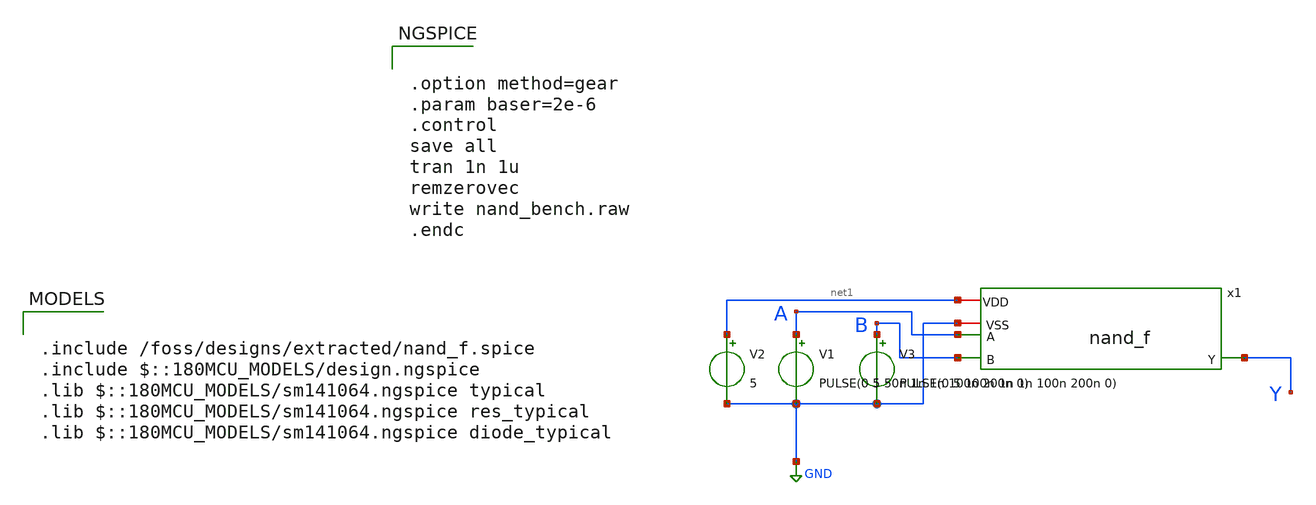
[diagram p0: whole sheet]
** sch_path: analog/xschem/nand_bench.sch
**.subckt nand_bench
V2 net1 GND 5
V1 A GND PULSE(0 5 50n 1n 1n 100n 200n 0)
V3 B GND PULSE(0 5 100n 1n 1n 100n 200n 0)
x1 net1 GND A B Y nand_f
**** begin user architecture code


.option method=gear
.param baser=2e-6
.control
save all
tran 1n 1u
remzerovec
write nand_bench.raw
.endc



.include /foss/designs/extracted/nand_f.spice
.include $::180MCU_MODELS/design.ngspice
.lib $::180MCU_MODELS/sm141064.ngspice typical
.lib $::180MCU_MODELS/sm141064.ngspice res_typical
.lib $::180MCU_MODELS/sm141064.ngspice diode_typical

**** end user architecture code
**.ends
.GLOBAL GND
.end
